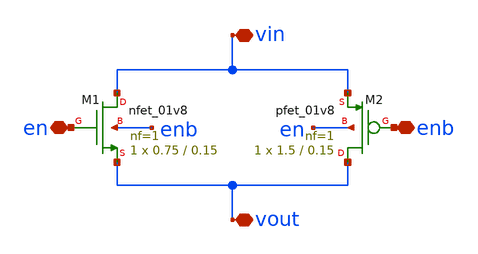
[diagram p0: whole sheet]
** sch_path: designs/tg.sch
**.subckt tg vin vout enb en
*.iopin vin
*.iopin vout
*.iopin enb
*.iopin en
XM1 vin en vout enb sky130_fd_pr__nfet_01v8 L=0.15 W=0.75 nf=1 ad='int((nf+1)/2) * W/nf * 0.29' as='int((nf+2)/2) * W/nf * 0.29'
+ pd='2*int((nf+1)/2) * (W/nf + 0.29)' ps='2*int((nf+2)/2) * (W/nf + 0.29)' nrd='0.29 / W' nrs='0.29 / W'
+ sa=0 sb=0 sd=0 mult=1 m=1
XM2 vout enb vin en sky130_fd_pr__pfet_01v8 L=0.15 W=1.5 nf=1 ad='int((nf+1)/2) * W/nf * 0.29' as='int((nf+2)/2) * W/nf * 0.29'
+ pd='2*int((nf+1)/2) * (W/nf + 0.29)' ps='2*int((nf+2)/2) * (W/nf + 0.29)' nrd='0.29 / W' nrs='0.29 / W'
+ sa=0 sb=0 sd=0 mult=1 m=1
**.ends
.end
